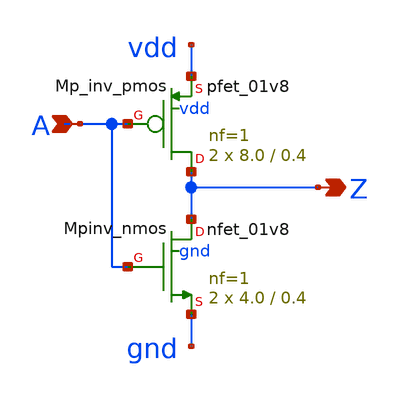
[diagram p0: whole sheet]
** sch_path: sram_2_16_scn4m/pinv_9.sch
**.subckt pinv_9 A Z
*.ipin A
*.opin Z
XMpinv_nmos Z A gnd gnd sky130_fd_pr__nfet_01v8 L=0.4 W=4.0 nf=1 ad='int((nf+1)/2) * W/nf * 0.29' as='int((nf+2)/2) * W/nf * 0.29'
+ pd='2*int((nf+1)/2) * (W/nf + 0.29)' ps='2*int((nf+2)/2) * (W/nf + 0.29)' nrd='0.29 / W' nrs='0.29 / W'
+ sa=0 sb=0 sd=0 mult=2 m=2
XMp_inv_pmos Z A vdd vdd sky130_fd_pr__pfet_01v8 L=0.4 W=8.0 nf=1 ad='int((nf+1)/2) * W/nf * 0.29' as='int((nf+2)/2) * W/nf * 0.29'
+ pd='2*int((nf+1)/2) * (W/nf + 0.29)' ps='2*int((nf+2)/2) * (W/nf + 0.29)' nrd='0.29 / W' nrs='0.29 / W'
+ sa=0 sb=0 sd=0 mult=2 m=2
**.ends
.end
